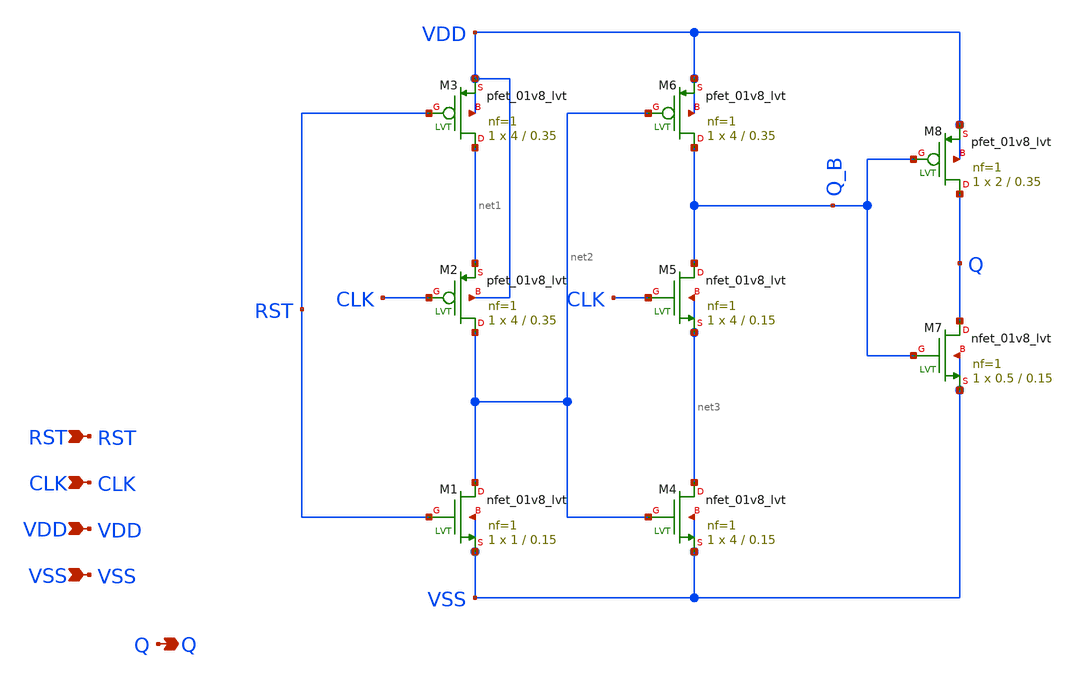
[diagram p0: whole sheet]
** sch_path: design/LELO_SVOD_SKY130A/LELO_TSPC_FULL.sch
**.subckt LELO_TSPC_FULL RST CLK VDD VSS Q
*.ipin RST
*.ipin CLK
*.ipin VDD
*.ipin VSS
*.opin Q
XM1 net2 RST VSS VSS sky130_fd_pr__nfet_01v8_lvt L=0.15 W=1 nf=1 ad='int((1 + 1)/2) * 1 / 1 * 0.29' as='int((1 + 2)/2) * 1 / 1 * 0.29'
+ pd='2*int((1 + 1)/2) * (1 / 1 + 0.29)' ps='2*int((1 + 2)/2) * (1 / 1 + 0.29)' nrd='0.29 / 1 ' nrs='0.29 / 1 '
+ sa=0 sb=0 sd=0 mult=1 m=1
XM2 net2 CLK net1 VDD sky130_fd_pr__pfet_01v8_lvt L=0.35 W=4 nf=1 ad='int((1 + 1)/2) * 4 / 1 * 0.29'
+ as='int((1 + 2)/2) * 4 / 1 * 0.29' pd='2*int((1 + 1)/2) * (4 / 1 + 0.29)' ps='2*int((1 + 2)/2) * (4 / 1 + 0.29)'
+ nrd='0.29 / 4 ' nrs='0.29 / 4 ' sa=0 sb=0 sd=0 mult=1 m=1
XM3 net1 RST VDD VDD sky130_fd_pr__pfet_01v8_lvt L=0.35 W=4 nf=1 ad='int((1 + 1)/2) * 4 / 1 * 0.29' as='int((1 + 2)/2) * 4 / 1 * 0.29'
+ pd='2*int((1 + 1)/2) * (4 / 1 + 0.29)' ps='2*int((1 + 2)/2) * (4 / 1 + 0.29)' nrd='0.29 / 4 ' nrs='0.29 / 4 '
+ sa=0 sb=0 sd=0 mult=1 m=1
XM4 net3 net2 VSS VSS sky130_fd_pr__nfet_01v8_lvt L=0.15 W=4 nf=1 ad='int((1 + 1)/2) * 4 / 1 * 0.29'
+ as='int((1 + 2)/2) * 4 / 1 * 0.29' pd='2*int((1 + 1)/2) * (4 / 1 + 0.29)' ps='2*int((1 + 2)/2) * (4 / 1 + 0.29)'
+ nrd='0.29 / 4 ' nrs='0.29 / 4 ' sa=0 sb=0 sd=0 mult=1 m=1
XM5 Q_B CLK net3 net3 sky130_fd_pr__nfet_01v8_lvt L=0.15 W=4 nf=1 ad='int((1 + 1)/2) * 4 / 1 * 0.29'
+ as='int((1 + 2)/2) * 4 / 1 * 0.29' pd='2*int((1 + 1)/2) * (4 / 1 + 0.29)' ps='2*int((1 + 2)/2) * (4 / 1 + 0.29)'
+ nrd='0.29 / 4 ' nrs='0.29 / 4 ' sa=0 sb=0 sd=0 mult=1 m=1
XM6 Q_B net2 VDD VDD sky130_fd_pr__pfet_01v8_lvt L=0.35 W=4 nf=1 ad='int((1 + 1)/2) * 4 / 1 * 0.29' as='int((1 + 2)/2) * 4 / 1 * 0.29'
+ pd='2*int((1 + 1)/2) * (4 / 1 + 0.29)' ps='2*int((1 + 2)/2) * (4 / 1 + 0.29)' nrd='0.29 / 4 ' nrs='0.29 / 4 '
+ sa=0 sb=0 sd=0 mult=1 m=1
XM7 Q Q_B VSS VSS sky130_fd_pr__nfet_01v8_lvt L=0.15 W=0.5 nf=1 ad='int((1 + 1)/2) * 0.5 / 1 * 0.29'
+ as='int((1 + 2)/2) * 0.5 / 1 * 0.29' pd='2*int((1 + 1)/2) * (0.5 / 1 + 0.29)' ps='2*int((1 + 2)/2) * (0.5 / 1 + 0.29)'
+ nrd='0.29 / 0.5 ' nrs='0.29 / 0.5 ' sa=0 sb=0 sd=0 mult=1 m=1
XM8 Q Q_B VDD VDD sky130_fd_pr__pfet_01v8_lvt L=0.35 W=2 nf=1 ad='int((1 + 1)/2) * 2 / 1 * 0.29' as='int((1 + 2)/2) * 2 / 1 * 0.29'
+ pd='2*int((1 + 1)/2) * (2 / 1 + 0.29)' ps='2*int((1 + 2)/2) * (2 / 1 + 0.29)' nrd='0.29 / 2 ' nrs='0.29 / 2 '
+ sa=0 sb=0 sd=0 mult=1 m=1
**.ends
.end
